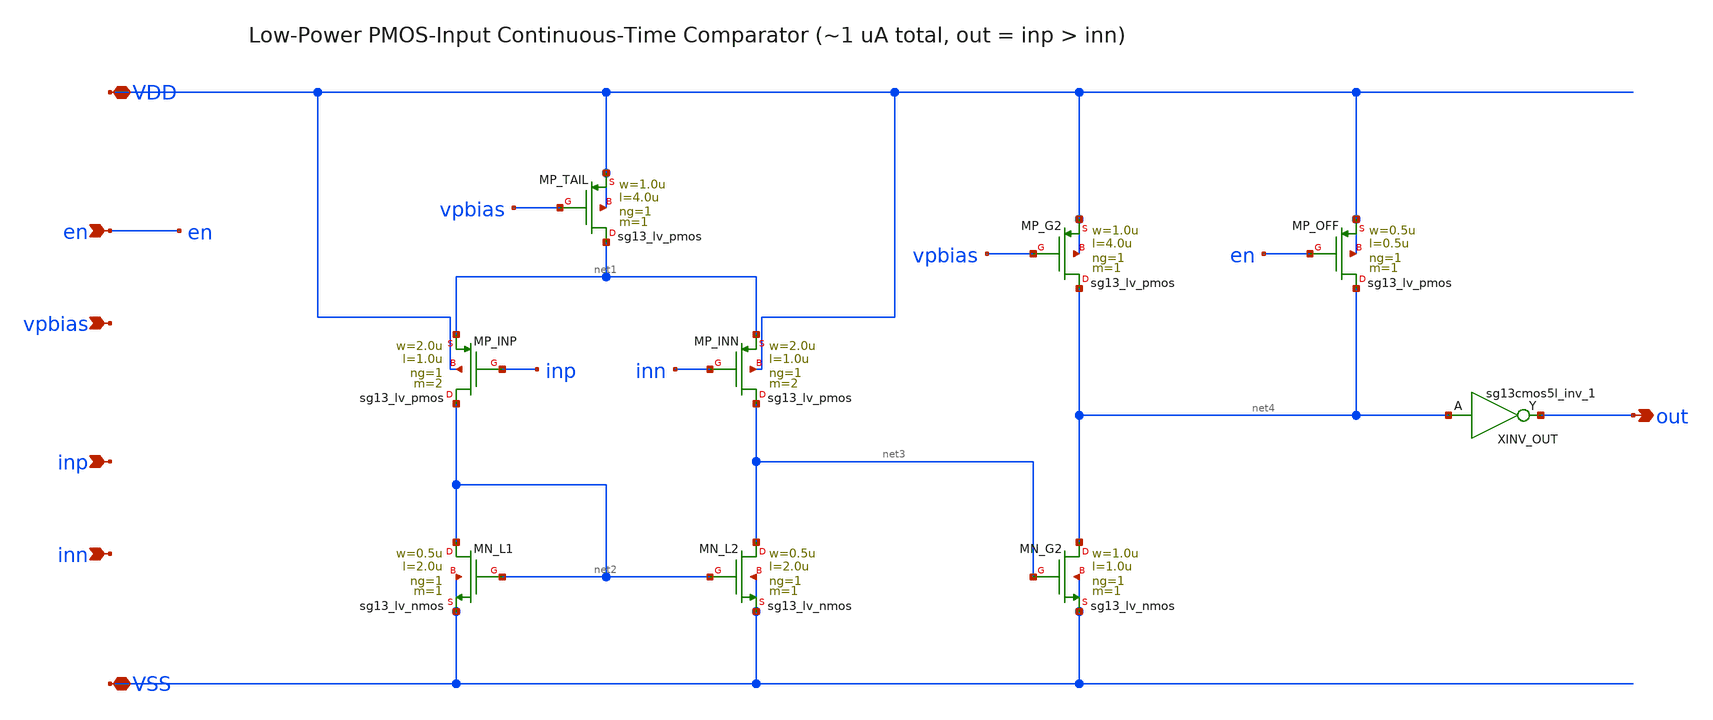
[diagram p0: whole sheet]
** sch_path: analog/osc_relax/comp.sch
**.subckt comp VDD VSS en vpbias inp inn out
*.iopin VDD
*.iopin VSS
*.ipin en
*.ipin vpbias
*.ipin inp
*.ipin inn
*.opin out
XMP_TAIL net1 vpbias VDD VDD sg13_lv_pmos w=1.0u l=4.0u ng=1 m=1 mm_ok=1
XMP_INP net2 inp net1 VDD sg13_lv_pmos w=2.0u l=1.0u ng=1 m=2 mm_ok=1
XMP_INN net3 inn net1 VDD sg13_lv_pmos w=2.0u l=1.0u ng=1 m=2 mm_ok=1
XMN_L1 net2 net2 VSS VSS sg13_lv_nmos w=0.5u l=2.0u ng=1 m=1 mm_ok=1
XMN_L2 net3 net2 VSS VSS sg13_lv_nmos w=0.5u l=2.0u ng=1 m=1 mm_ok=1
XMP_G2 net4 vpbias VDD VDD sg13_lv_pmos w=1.0u l=4.0u ng=1 m=1 mm_ok=1
XMN_G2 net4 net3 VSS VSS sg13_lv_nmos w=1.0u l=1.0u ng=1 m=1 mm_ok=1
XMP_OFF net4 en VDD VDD sg13_lv_pmos w=0.5u l=0.5u ng=1 m=1 mm_ok=1
XINV_OUT out net4 VDD VSS sg13cmos5l_inv_1
**.ends
.end
